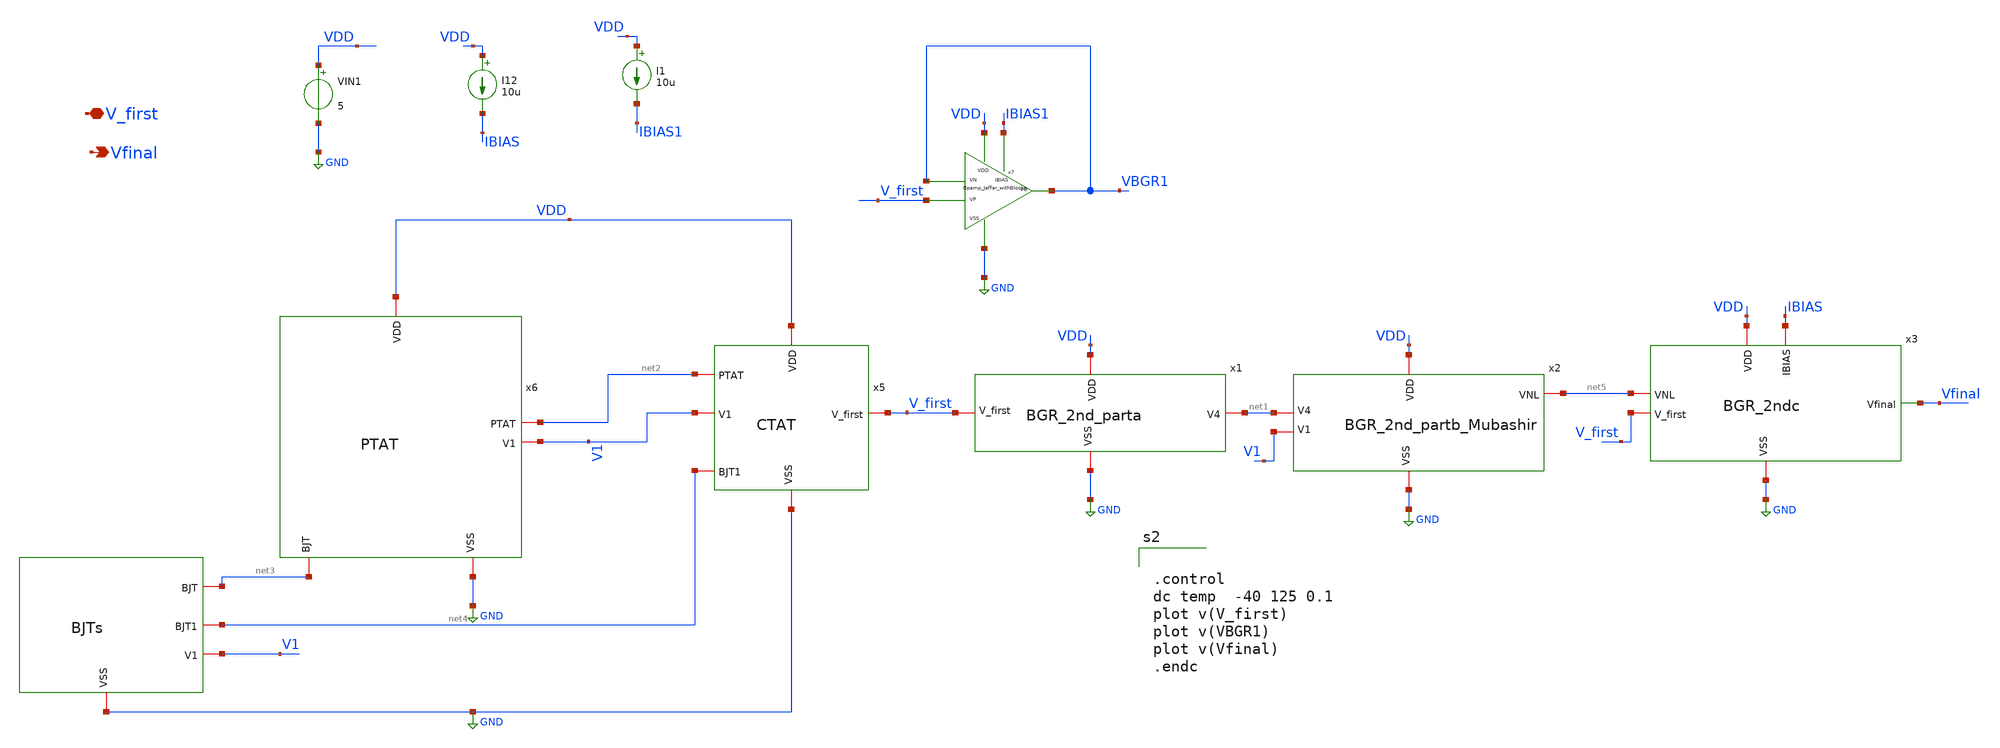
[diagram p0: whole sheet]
** sch_path: xschem/xschem_BGR_Top/BGR_Toplevel_tb.sch
**.subckt BGR_Toplevel_tb Vfinal V_first
*.opin Vfinal
*.iopin V_first
x1 VDD GND V_first net1 BGR_2nd_parta
x3 VDD GND net5 V_first IBIAS Vfinal BGR_2ndc
x2 VDD GND V1 net1 net5 BGR_2nd_partb_Mubashir
x4 net3 GND net4 V1 BJTs
x5 VDD net2 V1 V_first GND net4 CTAT
x6 VDD net2 V1 net3 GND PTAT
VIN1 VDD GND 5
I12 VDD IBIAS 10u
x7 VDD GND V_first VBGR1 VBGR1 IBIAS1 Opamp_Jaffar_withBlocks
I1 VDD IBIAS1 10u
**** begin user architecture code

** opencircuitdesign pdks install
.lib $::SKYWATER_MODELS/sky130.lib.spice tt




.control
dc temp  -40 125 0.1
plot v(V_first)
plot v(VBGR1)
plot v(Vfinal)
.endc


**** end user architecture code
**.ends
.GLOBAL GND
.end
